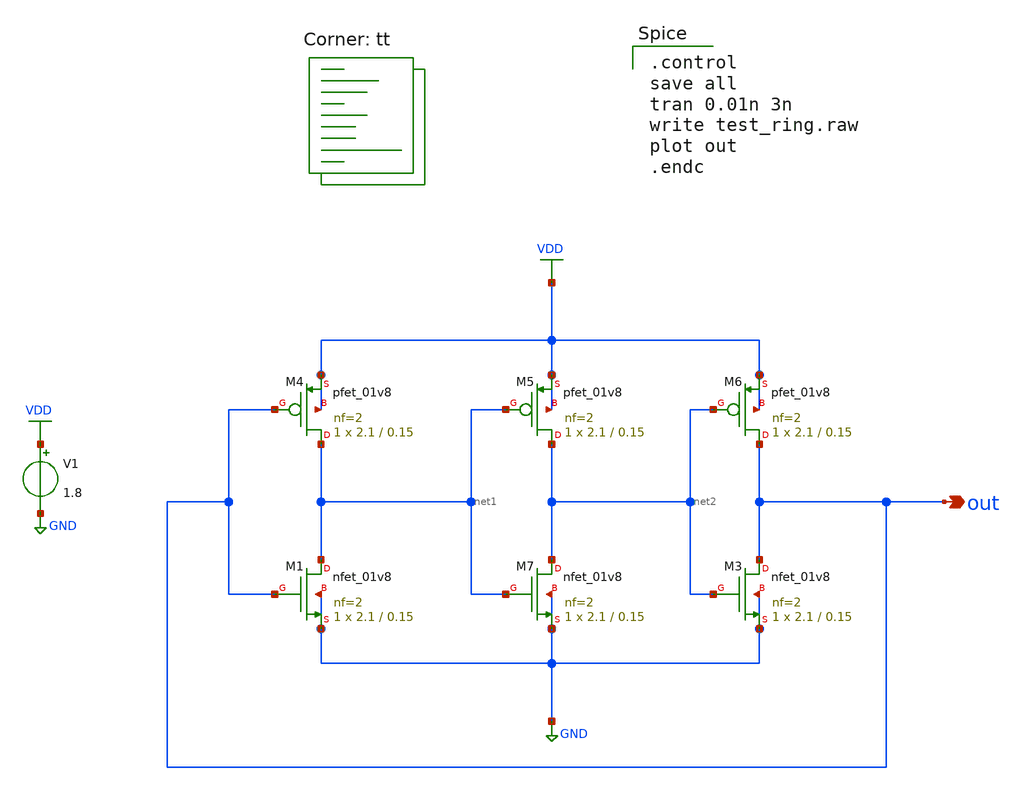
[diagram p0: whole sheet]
** sch_path: Ring_Oscillator.sch
**.subckt Ring_Oscillator out
*.opin out
XM1 net1 out GND GND sky130_fd_pr__nfet_01v8 L=0.15 W=2.1 nf=2 ad='int((nf+1)/2) * W/nf * 0.29' as='int((nf+2)/2) * W/nf * 0.29'
+ pd='2*int((nf+1)/2) * (W/nf + 0.29)' ps='2*int((nf+2)/2) * (W/nf + 0.29)' nrd='0.29 / W' nrs='0.29 / W'
+ sa=0 sb=0 sd=0 mult=1 m=1
XM3 out net2 GND GND sky130_fd_pr__nfet_01v8 L=0.15 W=2.1 nf=2 ad='int((nf+1)/2) * W/nf * 0.29' as='int((nf+2)/2) * W/nf * 0.29'
+ pd='2*int((nf+1)/2) * (W/nf + 0.29)' ps='2*int((nf+2)/2) * (W/nf + 0.29)' nrd='0.29 / W' nrs='0.29 / W'
+ sa=0 sb=0 sd=0 mult=1 m=1
XM4 net1 out VDD VDD sky130_fd_pr__pfet_01v8 L=0.15 W=2.1 nf=2 ad='int((nf+1)/2) * W/nf * 0.29' as='int((nf+2)/2) * W/nf * 0.29'
+ pd='2*int((nf+1)/2) * (W/nf + 0.29)' ps='2*int((nf+2)/2) * (W/nf + 0.29)' nrd='0.29 / W' nrs='0.29 / W'
+ sa=0 sb=0 sd=0 mult=1 m=1
XM5 net2 net1 VDD VDD sky130_fd_pr__pfet_01v8 L=0.15 W=2.1 nf=2 ad='int((nf+1)/2) * W/nf * 0.29' as='int((nf+2)/2) * W/nf * 0.29'
+ pd='2*int((nf+1)/2) * (W/nf + 0.29)' ps='2*int((nf+2)/2) * (W/nf + 0.29)' nrd='0.29 / W' nrs='0.29 / W'
+ sa=0 sb=0 sd=0 mult=1 m=1
XM6 out net2 VDD VDD sky130_fd_pr__pfet_01v8 L=0.15 W=2.1 nf=2 ad='int((nf+1)/2) * W/nf * 0.29' as='int((nf+2)/2) * W/nf * 0.29'
+ pd='2*int((nf+1)/2) * (W/nf + 0.29)' ps='2*int((nf+2)/2) * (W/nf + 0.29)' nrd='0.29 / W' nrs='0.29 / W'
+ sa=0 sb=0 sd=0 mult=1 m=1
XM7 net2 net1 GND GND sky130_fd_pr__nfet_01v8 L=0.15 W=2.1 nf=2 ad='int((nf+1)/2) * W/nf * 0.29' as='int((nf+2)/2) * W/nf * 0.29'
+ pd='2*int((nf+1)/2) * (W/nf + 0.29)' ps='2*int((nf+2)/2) * (W/nf + 0.29)' nrd='0.29 / W' nrs='0.29 / W'
+ sa=0 sb=0 sd=0 mult=1 m=1
V1 VDD GND 1.8
**** begin user architecture code

.control
save all
tran 0.01n 3n
write test_ring.raw
plot out
.endc

.lib $::SKYWATER_MODELS/sky130.lib.spice tt
**** end user architecture code
**.ends
.GLOBAL GND
.GLOBAL VDD
.end
